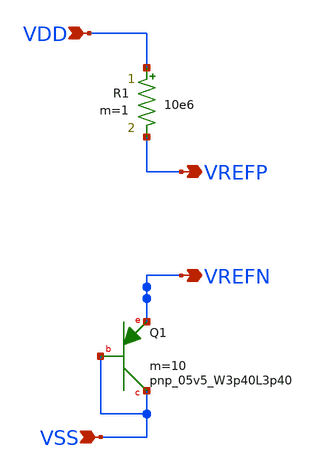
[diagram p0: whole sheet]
** sch_path: design/CNR_GR02_SKY130NM/CNR_GR02.sch
**.subckt CNR_GR02 VDD VSS VREFP VREFN
*.ipin VDD
*.ipin VSS
*.opin VREFP
*.opin VREFN
R1 VDD VREFP 10e6 m=1
XQ1 VSS VSS VREFN sky130_fd_pr__pnp_05v5_W3p40L3p40 m=10
**.ends
.end
